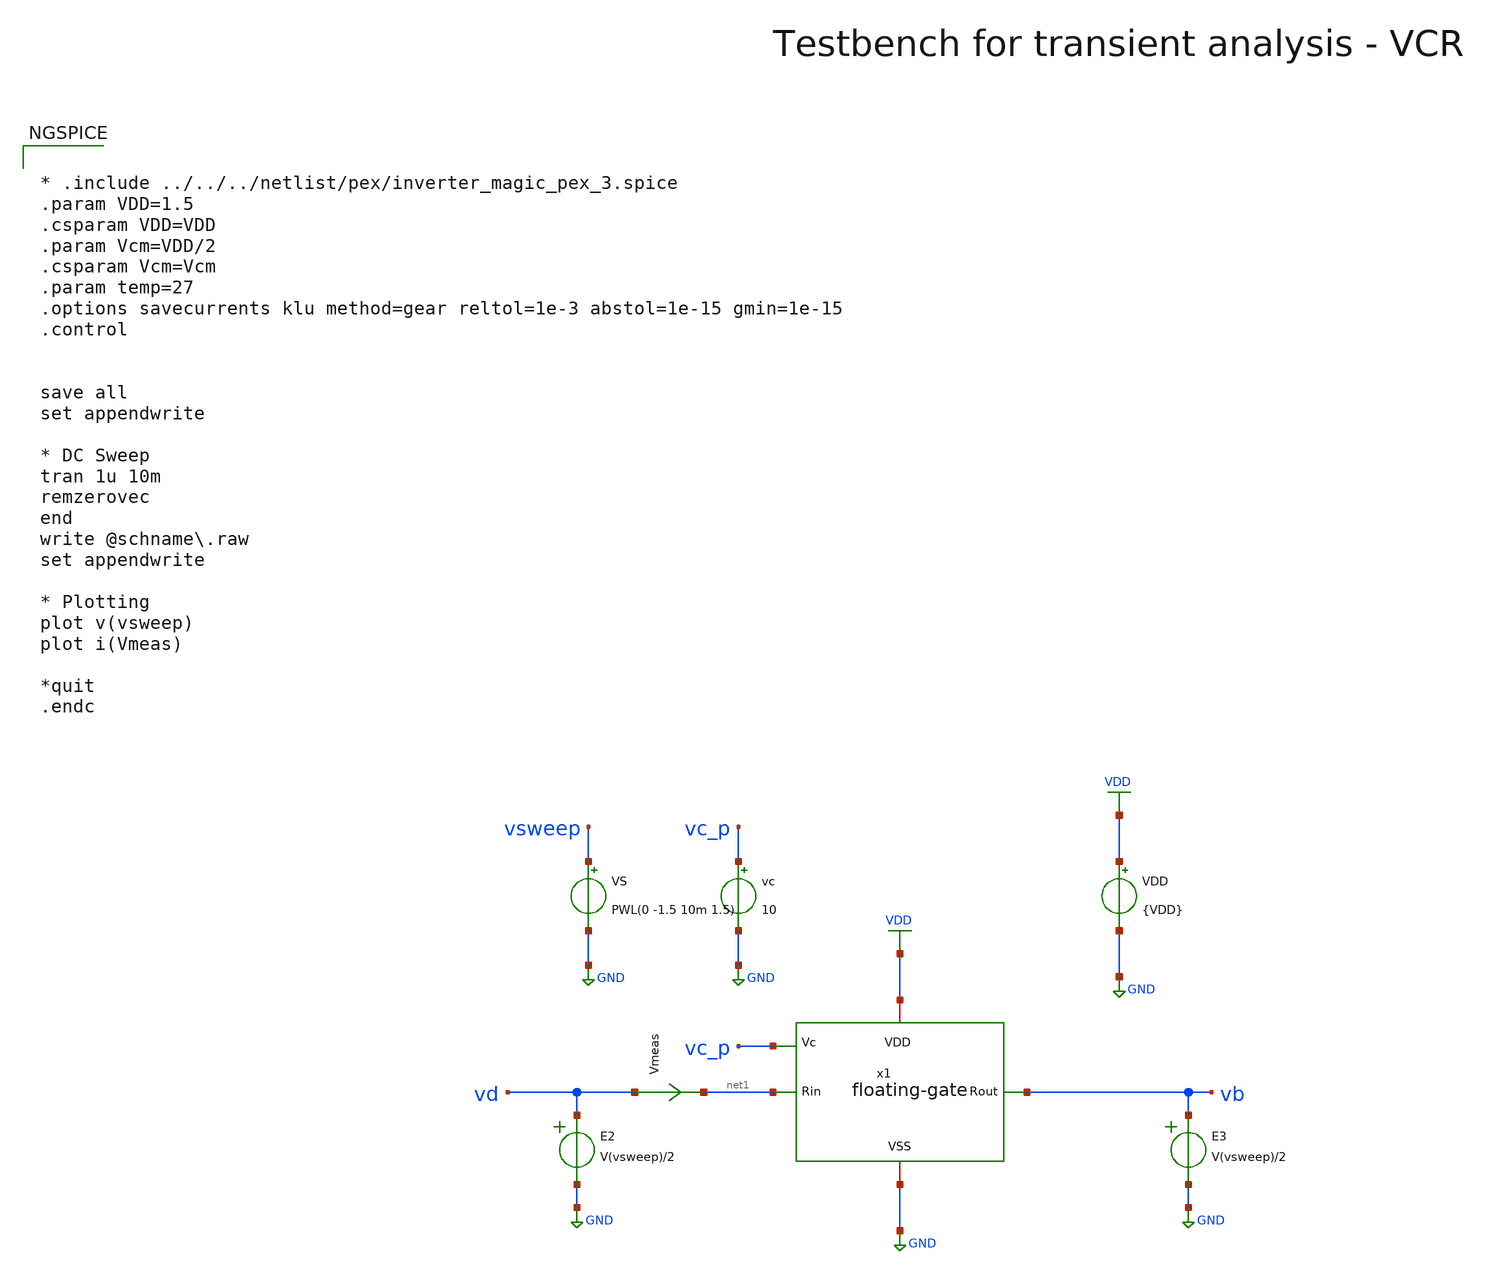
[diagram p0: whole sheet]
** sch_path: macros/heichips26_analog_project/macros/floating-gate/testbenches/xschem/res_tb_tran2.sch
**.subckt res_tb_tran2
VDD VDD GND {VDD}
VS vsweep GND PWL(0 -1.5 10m 1.5)
Vmeas vd net1 0
.save i(vmeas)
E2 vd GND VOL=' V(vsweep)/2 '
E3 vb GND VOL=' V(vsweep)/2 '
vc vc_p GND 10
x1 net1 VDD GND vb vc_p floating-gate
**** begin user architecture code

.lib cornerMOSlv.lib mos_tt
.lib cornerMOShv.lib mos_tt
.lib cornerRES.lib res_typ
.lib cornerDIO.lib dio_tt



* .include ../../../netlist/pex/inverter_magic_pex_3.spice
.param VDD=1.5
.csparam VDD=VDD
.param Vcm=VDD/2
.csparam Vcm=Vcm
.param temp=27
.options savecurrents klu method=gear reltol=1e-3 abstol=1e-15 gmin=1e-15
.control


save all
set appendwrite

* DC Sweep
tran 1u 10m
remzerovec
end
write @schname\.raw
set appendwrite

* Plotting
plot v(vsweep)
plot i(Vmeas)

*quit
.endc


**** end user architecture code
**.ends

* expanding   symbol:
*+  /home/raiku/k/heichips26-voltage-controlled-resistor/macros/heichips26_analog_project/macros/floating-gate/schematic/xschem/floating-gate.sym # of pins=5
** sym_path: macros/heichips26_analog_project/macros/floating-gate/schematic/xschem/floating-gate.sym
** sch_path: macros/heichips26_analog_project/macros/floating-gate/schematic/xschem/floating-gate.sch
.subckt floating-gate Rin VDD VSS Rout Vc
*.iopin VDD
*.ipin Rin
*.opin Rout
*.ipin Vc
*.iopin VSS
*.opin Rout
*.ipin Vc
*.ipin Rin
*.iopin VSS
XM2 net2 net2 net1 net6 sg13_hv_nmos w=7u l=4u ng=20 m=1 mm_ok=1
XM4 net3 net3 net1 net6 sg13_hv_nmos w=7u l=4u ng=20 m=1 mm_ok=1
XM3 net1 net4 net5 net6 sg13_hv_nmos w=7u l=4u ng=20 m=1 mm_ok=1
XM1 net2 net4 net5 net6 sg13_hv_nmos w=7u l=4u ng=20 m=1 mm_ok=1
XM5 Rin Vc Rout VSS sg13_hv_nmos w=7u l=4u ng=20 m=1 mm_ok=1
.ends

.GLOBAL GND
.GLOBAL VDD
.end
